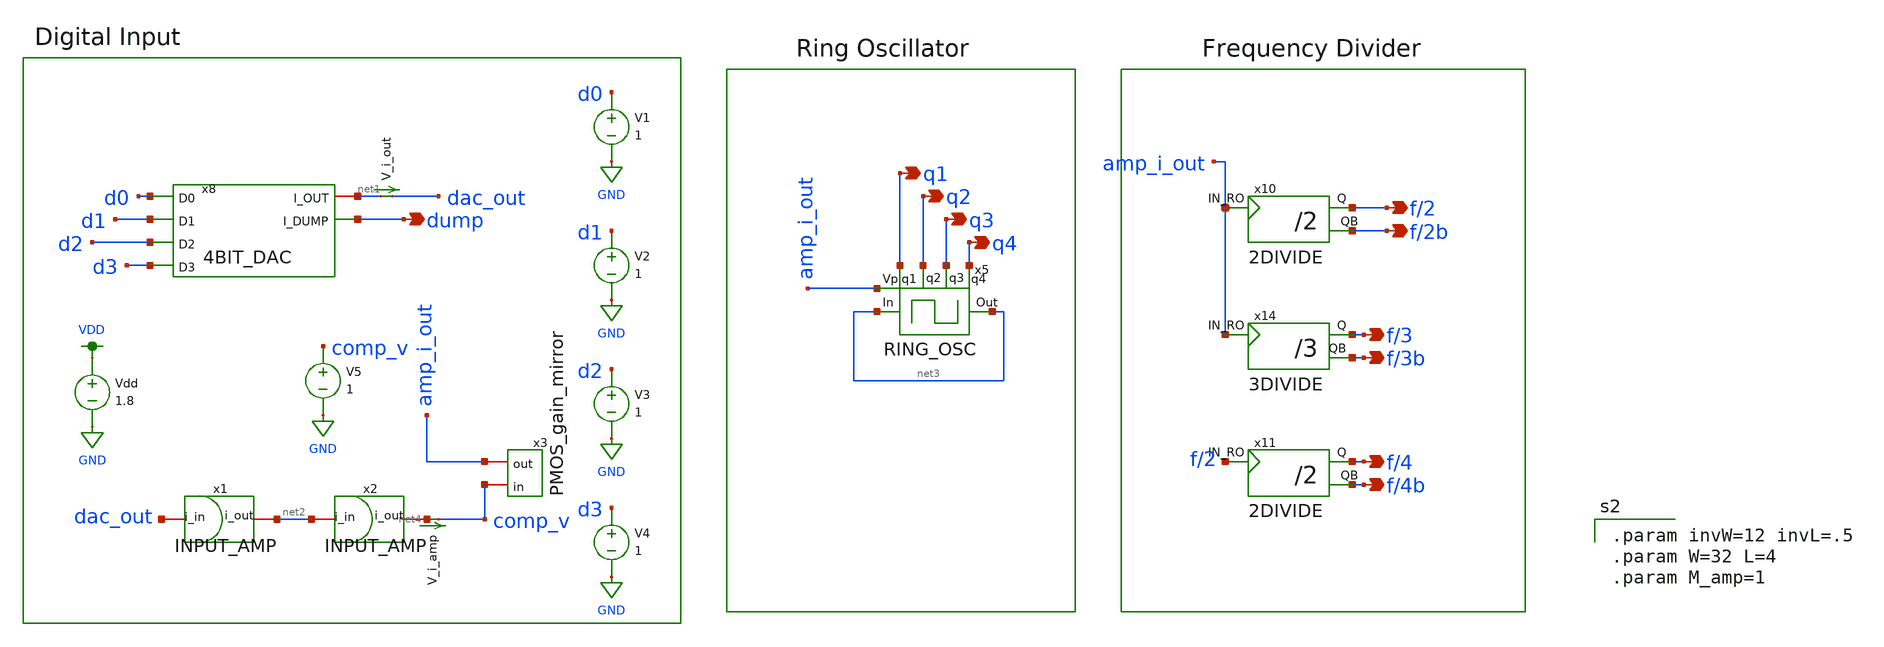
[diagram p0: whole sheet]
** sch_path: schemas/transient_testbench.sch
**.subckt transient_testbench dump f/2 f/4 f/3 f/3b f/4b f/2b q1 q2 q3 q4
*.opin dump
*.opin f/2
*.opin f/4
*.opin f/3
*.opin f/3b
*.opin f/4b
*.opin f/2b
*.opin q1
*.opin q2
*.opin q3
*.opin q4
x8 net1 dump d1 d0 d2 d3 4BIT_DAC
x10 f/2 f/2b amp_i_out 2DIVIDE
x11 f/4 f/4b f/2 2DIVIDE
V_i_out net1 dac_out 0
.save i(v_i_out)
x14 f/3 f/3b amp_i_out 3DIVIDE
V2 d1 GND 1
V1 d0 GND 1
V3 d2 GND 1
V4 d3 GND 1
x1 dac_out net2 INPUT_AMP
x2 net2 net4 INPUT_AMP
x5 q4 q1 q2 q3 net3 net3 amp_i_out RING_OSC
V_i_amp net4 comp_v 0
.save i(v_i_amp)
Vdd VDD GND 1.8
V5 comp_v GND 1
x3 amp_i_out comp_v PMOS_gain_mirror
**** begin user architecture code

.option wnflag=1
.lib ~/skywater/skywater-pdk/libraries/sky130_fd_pr_ngspice/latest/models/sky130.lib.spice tt




.param V1=1.8 V2=1.8 V3=1.8 V4=1.8

.tran 0.01n 30n
.save i(V_i_out) i(V_i_amp) v(RO_out) v(V_out) v(f/2) v(f/4) v(f/3) v(q1) v(q2) v(q3) v(q4)

.control
run
plot i(V_i_amp) i(V_i_out)
plot v(q1) v(q2) v(q3) v(q4)
.endc



.param invW=12 invL=.5
.param W=32 L=4
.param M_amp=1


**** end user architecture code
**.ends
.GLOBAL GND
.GLOBAL VDD
.end
